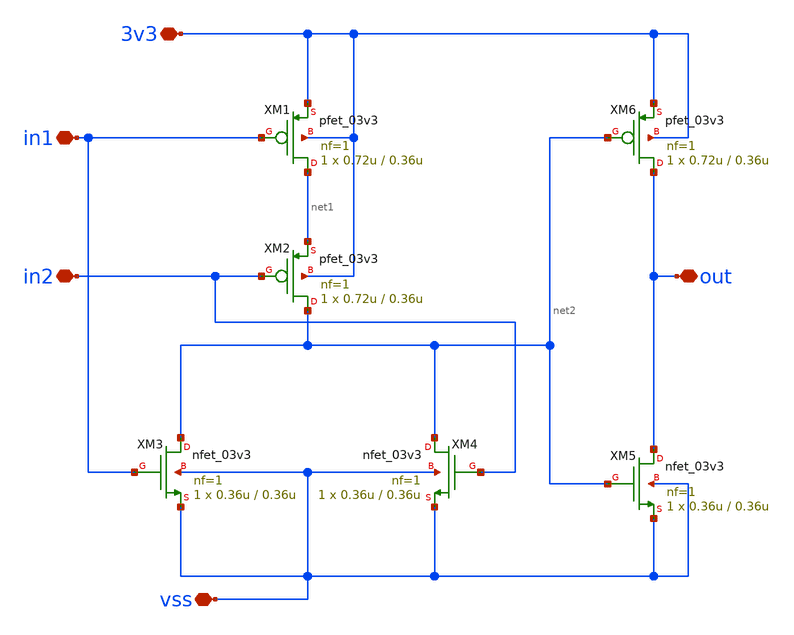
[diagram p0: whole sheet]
** sch_path: PLL/analog/schematics/2_input_or.sch
**.subckt 2_input_or in1 in2 out 3v3 vss
*.iopin in1
*.iopin in2
*.iopin out
*.iopin 3v3
*.iopin vss
XM1 net1 in1 3v3 3v3 pfet_03v3 L=0.36u W=0.72u nf=1 ad='int((nf+1)/2) * W/nf * 0.18u' as='int((nf+2)/2) * W/nf * 0.18u'
+ pd='2*int((nf+1)/2) * (W/nf + 0.18u)' ps='2*int((nf+2)/2) * (W/nf + 0.18u)' nrd='0.18u / W' nrs='0.18u / W'
+ sa=0 sb=0 sd=0 m=1
XM2 net2 in2 net1 3v3 pfet_03v3 L=0.36u W=0.72u nf=1 ad='int((nf+1)/2) * W/nf * 0.18u' as='int((nf+2)/2) * W/nf * 0.18u'
+ pd='2*int((nf+1)/2) * (W/nf + 0.18u)' ps='2*int((nf+2)/2) * (W/nf + 0.18u)' nrd='0.18u / W' nrs='0.18u / W'
+ sa=0 sb=0 sd=0 m=1
XM3 net2 in1 vss vss nfet_03v3 L=0.36u W=0.36u nf=1 ad='int((nf+1)/2) * W/nf * 0.18u' as='int((nf+2)/2) * W/nf * 0.18u'
+ pd='2*int((nf+1)/2) * (W/nf + 0.18u)' ps='2*int((nf+2)/2) * (W/nf + 0.18u)' nrd='0.18u / W' nrs='0.18u / W'
+ sa=0 sb=0 sd=0 m=1
XM4 net2 in2 vss vss nfet_03v3 L=0.36u W=0.36u nf=1 ad='int((nf+1)/2) * W/nf * 0.18u' as='int((nf+2)/2) * W/nf * 0.18u'
+ pd='2*int((nf+1)/2) * (W/nf + 0.18u)' ps='2*int((nf+2)/2) * (W/nf + 0.18u)' nrd='0.18u / W' nrs='0.18u / W'
+ sa=0 sb=0 sd=0 m=1
XM5 out net2 vss vss nfet_03v3 L=0.36u W=0.36u nf=1 ad='int((nf+1)/2) * W/nf * 0.18u' as='int((nf+2)/2) * W/nf * 0.18u'
+ pd='2*int((nf+1)/2) * (W/nf + 0.18u)' ps='2*int((nf+2)/2) * (W/nf + 0.18u)' nrd='0.18u / W' nrs='0.18u / W'
+ sa=0 sb=0 sd=0 m=1
XM6 out net2 3v3 3v3 pfet_03v3 L=0.36u W=0.72u nf=1 ad='int((nf+1)/2) * W/nf * 0.18u' as='int((nf+2)/2) * W/nf * 0.18u'
+ pd='2*int((nf+1)/2) * (W/nf + 0.18u)' ps='2*int((nf+2)/2) * (W/nf + 0.18u)' nrd='0.18u / W' nrs='0.18u / W'
+ sa=0 sb=0 sd=0 m=1
**.ends
.end
